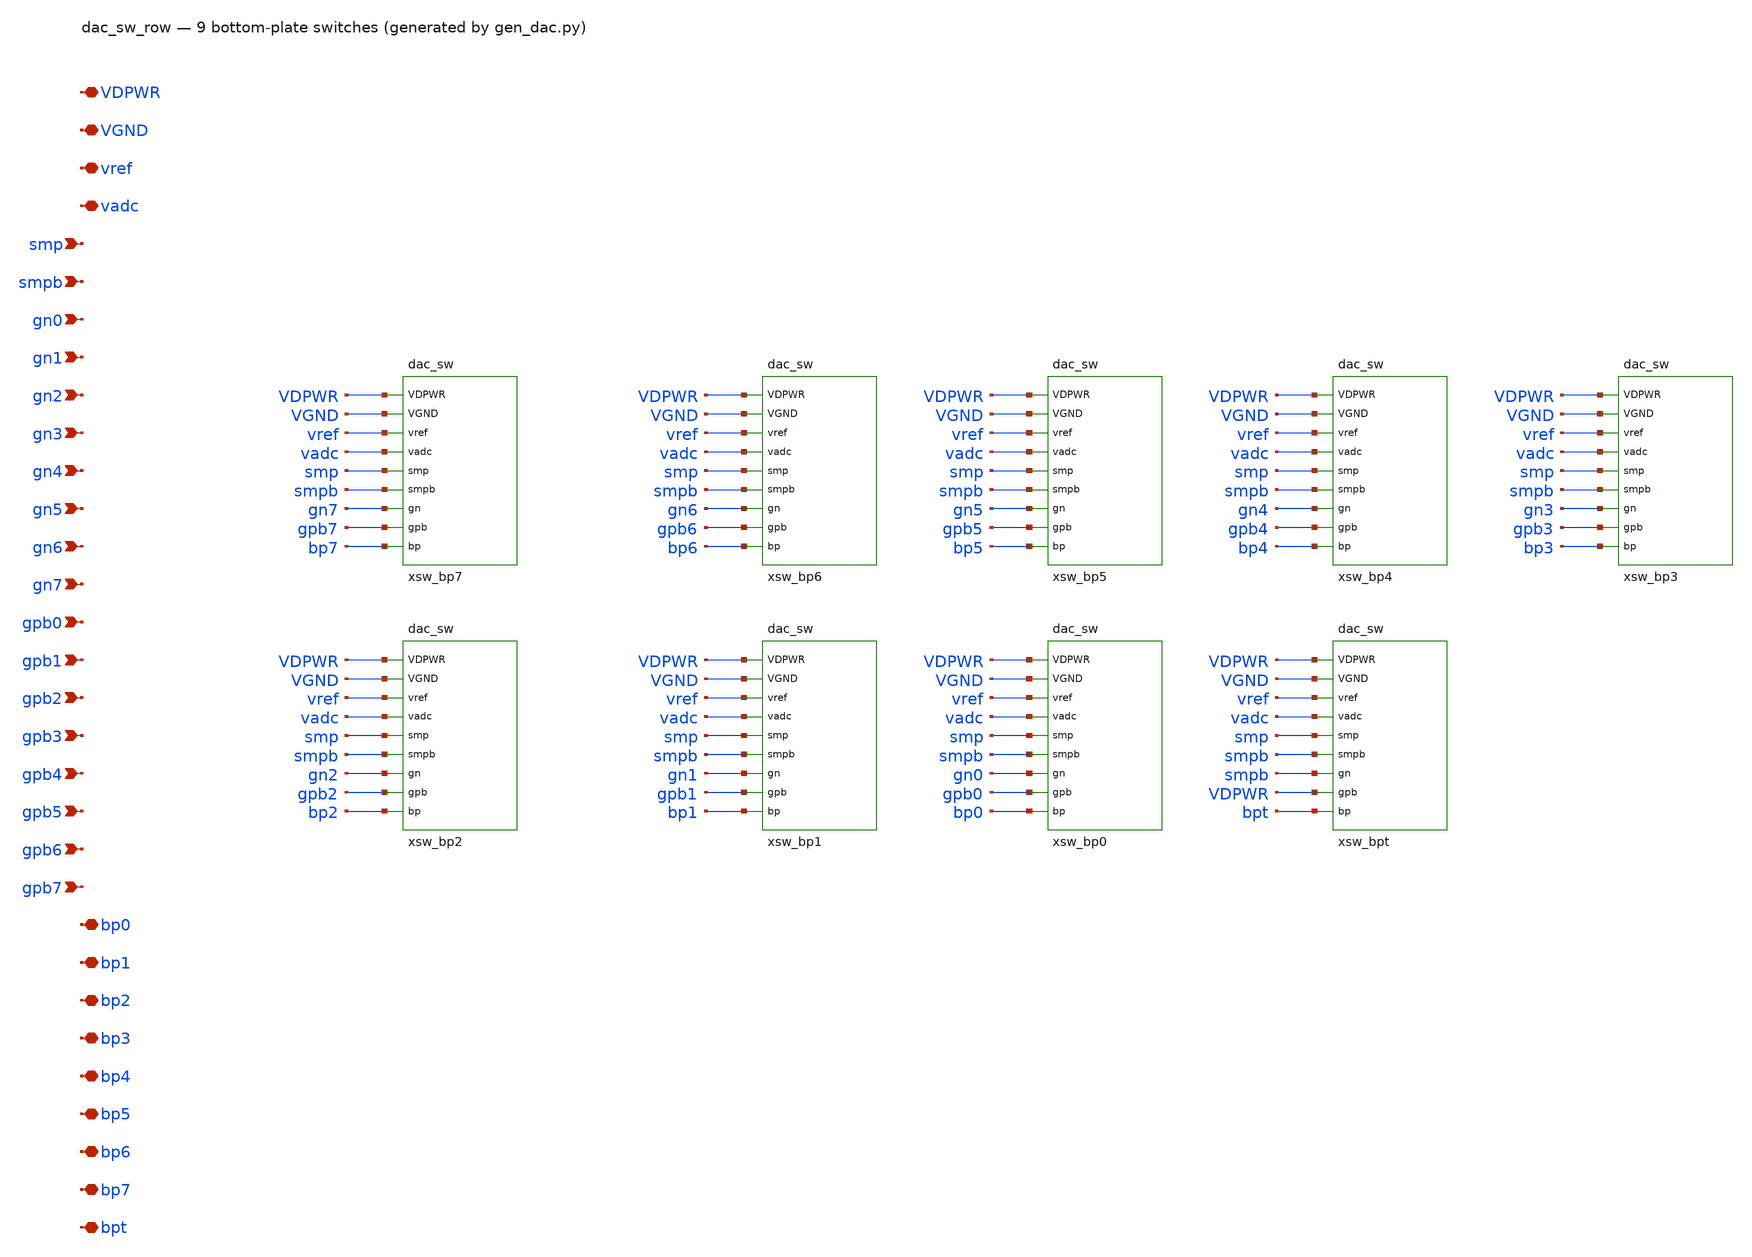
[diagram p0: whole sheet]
** sch_path: xschem/dac_sw_row.sch
**.subckt dac_sw_row VDPWR VGND vref vadc smp smpb gn0 gn1 gn2 gn3 gn4 gn5 gn6 gn7 gpb0 gpb1 gpb2
*+ gpb3 gpb4 gpb5 gpb6 gpb7 bp0 bp1 bp2 bp3 bp4 bp5 bp6 bp7 bpt
*.iopin VDPWR
*.iopin VGND
*.iopin vref
*.iopin vadc
*.ipin smp
*.ipin smpb
*.ipin gn0
*.ipin gn1
*.ipin gn2
*.ipin gn3
*.ipin gn4
*.ipin gn5
*.ipin gn6
*.ipin gn7
*.ipin gpb0
*.ipin gpb1
*.ipin gpb2
*.ipin gpb3
*.ipin gpb4
*.ipin gpb5
*.ipin gpb6
*.ipin gpb7
*.iopin bp0
*.iopin bp1
*.iopin bp2
*.iopin bp3
*.iopin bp4
*.iopin bp5
*.iopin bp6
*.iopin bp7
*.iopin bpt
xsw_bp7 VDPWR VGND vref vadc smp smpb gn7 gpb7 bp7 dac_sw
xsw_bp6 VDPWR VGND vref vadc smp smpb gn6 gpb6 bp6 dac_sw
xsw_bp5 VDPWR VGND vref vadc smp smpb gn5 gpb5 bp5 dac_sw
xsw_bp4 VDPWR VGND vref vadc smp smpb gn4 gpb4 bp4 dac_sw
xsw_bp3 VDPWR VGND vref vadc smp smpb gn3 gpb3 bp3 dac_sw
xsw_bp2 VDPWR VGND vref vadc smp smpb gn2 gpb2 bp2 dac_sw
xsw_bp1 VDPWR VGND vref vadc smp smpb gn1 gpb1 bp1 dac_sw
xsw_bp0 VDPWR VGND vref vadc smp smpb gn0 gpb0 bp0 dac_sw
xsw_bpt VDPWR VGND vref vadc smp smpb smpb VDPWR bpt dac_sw
**.ends

* expanding   symbol:  dac_sw.sym # of pins=9
** sym_path: xschem/dac_sw.sym
** sch_path: xschem/dac_sw.sch
.subckt dac_sw VDPWR VGND vref vadc smp smpb gn gpb bp
*.iopin VDPWR
*.iopin VGND
*.iopin vref
*.iopin vadc
*.ipin smp
*.ipin smpb
*.ipin gn
*.ipin gpb
*.iopin bp
XMSG bp gn VGND VGND sky130_fd_pr__nfet_01v8 L=0.15 W=1 nf=1 ad='int((1 + 1)/2) * 1 / 1 * 0.29' as='int((1 + 2)/2) * 1 / 1 * 0.29'
+ pd='2*int((1 + 1)/2) * (1 / 1 + 0.29)' ps='2*int((1 + 2)/2) * (1 / 1 + 0.29)' nrd='0.29 / 1 ' nrs='0.29 / 1 '
+ sa=0 sb=0 sd=0 mult=1 m=1
XMSR bp gpb vref VDPWR sky130_fd_pr__pfet_01v8_lvt L=0.35 W=4 nf=1 ad='int((1 + 1)/2) * 4 / 1 * 0.29'
+ as='int((1 + 2)/2) * 4 / 1 * 0.29' pd='2*int((1 + 1)/2) * (4 / 1 + 0.29)' ps='2*int((1 + 2)/2) * (4 / 1 + 0.29)'
+ nrd='0.29 / 4 ' nrs='0.29 / 4 ' sa=0 sb=0 sd=0 mult=1 m=1
XMSN bp smp vadc VGND sky130_fd_pr__nfet_01v8 L=0.15 W=1 nf=1 ad='int((1 + 1)/2) * 1 / 1 * 0.29' as='int((1 + 2)/2) * 1 / 1 * 0.29'
+ pd='2*int((1 + 1)/2) * (1 / 1 + 0.29)' ps='2*int((1 + 2)/2) * (1 / 1 + 0.29)' nrd='0.29 / 1 ' nrs='0.29 / 1 '
+ sa=0 sb=0 sd=0 mult=1 m=1
XMSP bp smpb vadc VDPWR sky130_fd_pr__pfet_01v8_lvt L=0.35 W=2 nf=1 ad='int((1 + 1)/2) * 2 / 1 * 0.29'
+ as='int((1 + 2)/2) * 2 / 1 * 0.29' pd='2*int((1 + 1)/2) * (2 / 1 + 0.29)' ps='2*int((1 + 2)/2) * (2 / 1 + 0.29)'
+ nrd='0.29 / 2 ' nrs='0.29 / 2 ' sa=0 sb=0 sd=0 mult=1 m=1
.ends

.end
